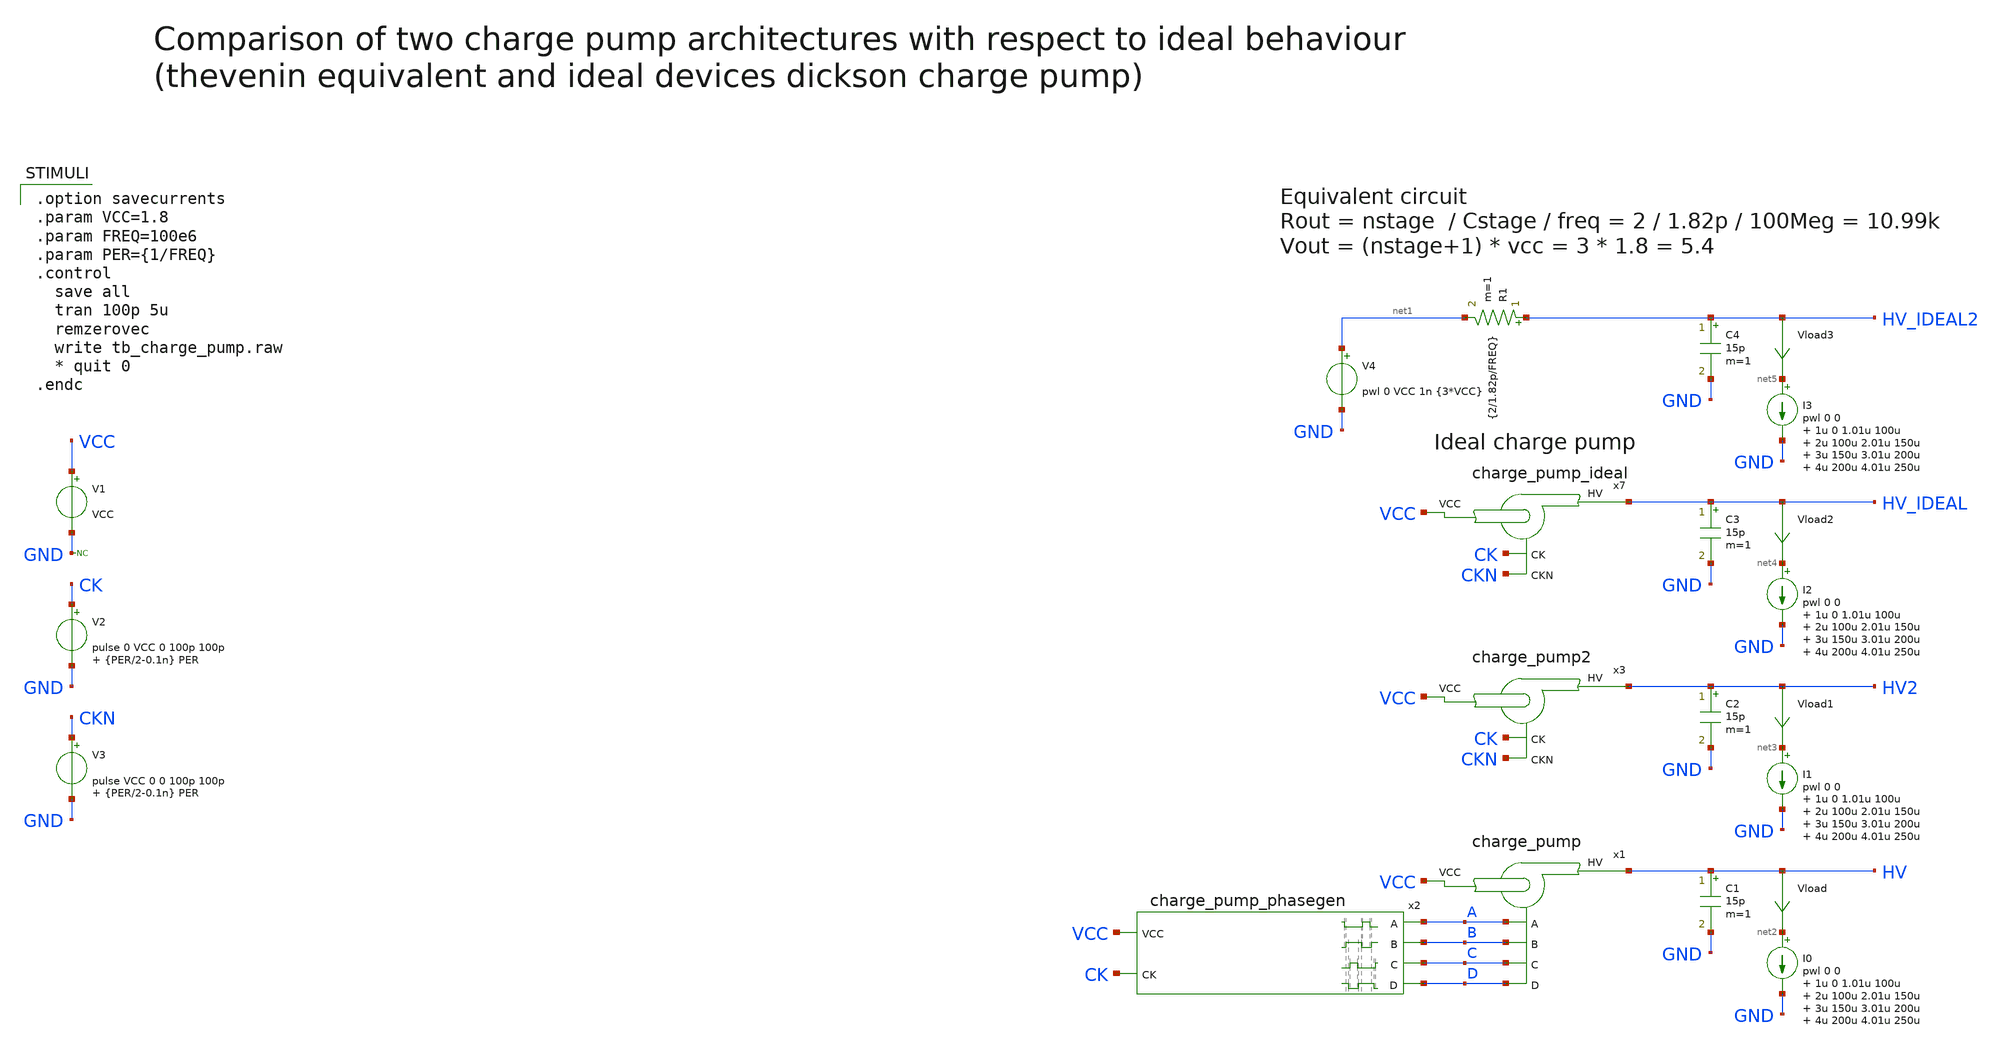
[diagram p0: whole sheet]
** sch_path: sky130_tests/tb_charge_pump.sch
* Copyright 2021 Stefan Frederik Schippers
* Licensed under the Apache License, Version 2.0 (the "License");
* you may not use this file except in compliance with the License.
* You may obtain a copy of the License at
* https://www.apache.org/licenses/LICENSE-2.0
* Unless required by applicable law or agreed to in writing, software
* distributed under the License is distributed on an "AS IS" BASIS,
* WITHOUT WARRANTIES OR CONDITIONS OF ANY KIND, either express or implied.
* See the License for the specific language governing permissions and
* limitations under the License.
.lib $::SKYWATER_MODELS/sky130.lib.spice tt
.include $::SKYWATER_STDCELLS/sky130_fd_sc_hd.spice

**.subckt tb_charge_pump
x1 VCC HV A B C D charge_pump
x2 A B C CK D VCC charge_pump_phasegen
V1 VCC GND VCC
V2 CK GND pulse 0 VCC 0 100p 100p {PER/2-0.1n} PER
C1 HV GND 15p m=1
I0 net2 GND pwl 0 0 1u 0 1.01u 100u 2u 100u 2.01u 150u 3u 150u 3.01u 200u 4u 200u 4.01u 250u
Vload HV net2 0
.save i(vload)
x3 VCC HV2 CK CKN charge_pump2
V3 CKN GND pulse VCC 0 0 100p 100p {PER/2-0.1n} PER
C2 HV2 GND 15p m=1
I1 net3 GND pwl 0 0 1u 0 1.01u 100u 2u 100u 2.01u 150u 3u 150u 3.01u 200u 4u 200u 4.01u 250u
Vload1 HV2 net3 0
.save i(vload1)
* noconn GND
C3 HV_IDEAL GND 15p m=1
Vload2 HV_IDEAL net4 0
.save i(vload2)
x7 VCC HV_IDEAL CK CKN charge_pump_ideal
I2 net4 GND pwl 0 0 1u 0 1.01u 100u 2u 100u 2.01u 150u 3u 150u 3.01u 200u 4u 200u 4.01u 250u
V4 net1 GND pwl 0 VCC 1n {3*VCC}
R1 HV_IDEAL2 net1 {2/1.82p/FREQ} m=1
C4 HV_IDEAL2 GND 15p m=1
Vload3 HV_IDEAL2 net5 0
.save i(vload3)
I3 net5 GND pwl 0 0 1u 0 1.01u 100u 2u 100u 2.01u 150u 3u 150u 3.01u 200u 4u 200u 4.01u 250u
**** begin user architecture code

.option savecurrents
.param VCC=1.8
.param FREQ=100e6
.param PER={1/FREQ}
.control
  save all
  tran 100p 5u
  remzerovec
  write tb_charge_pump.raw
  * quit 0
.endc


**** end user architecture code
**.ends
.end
